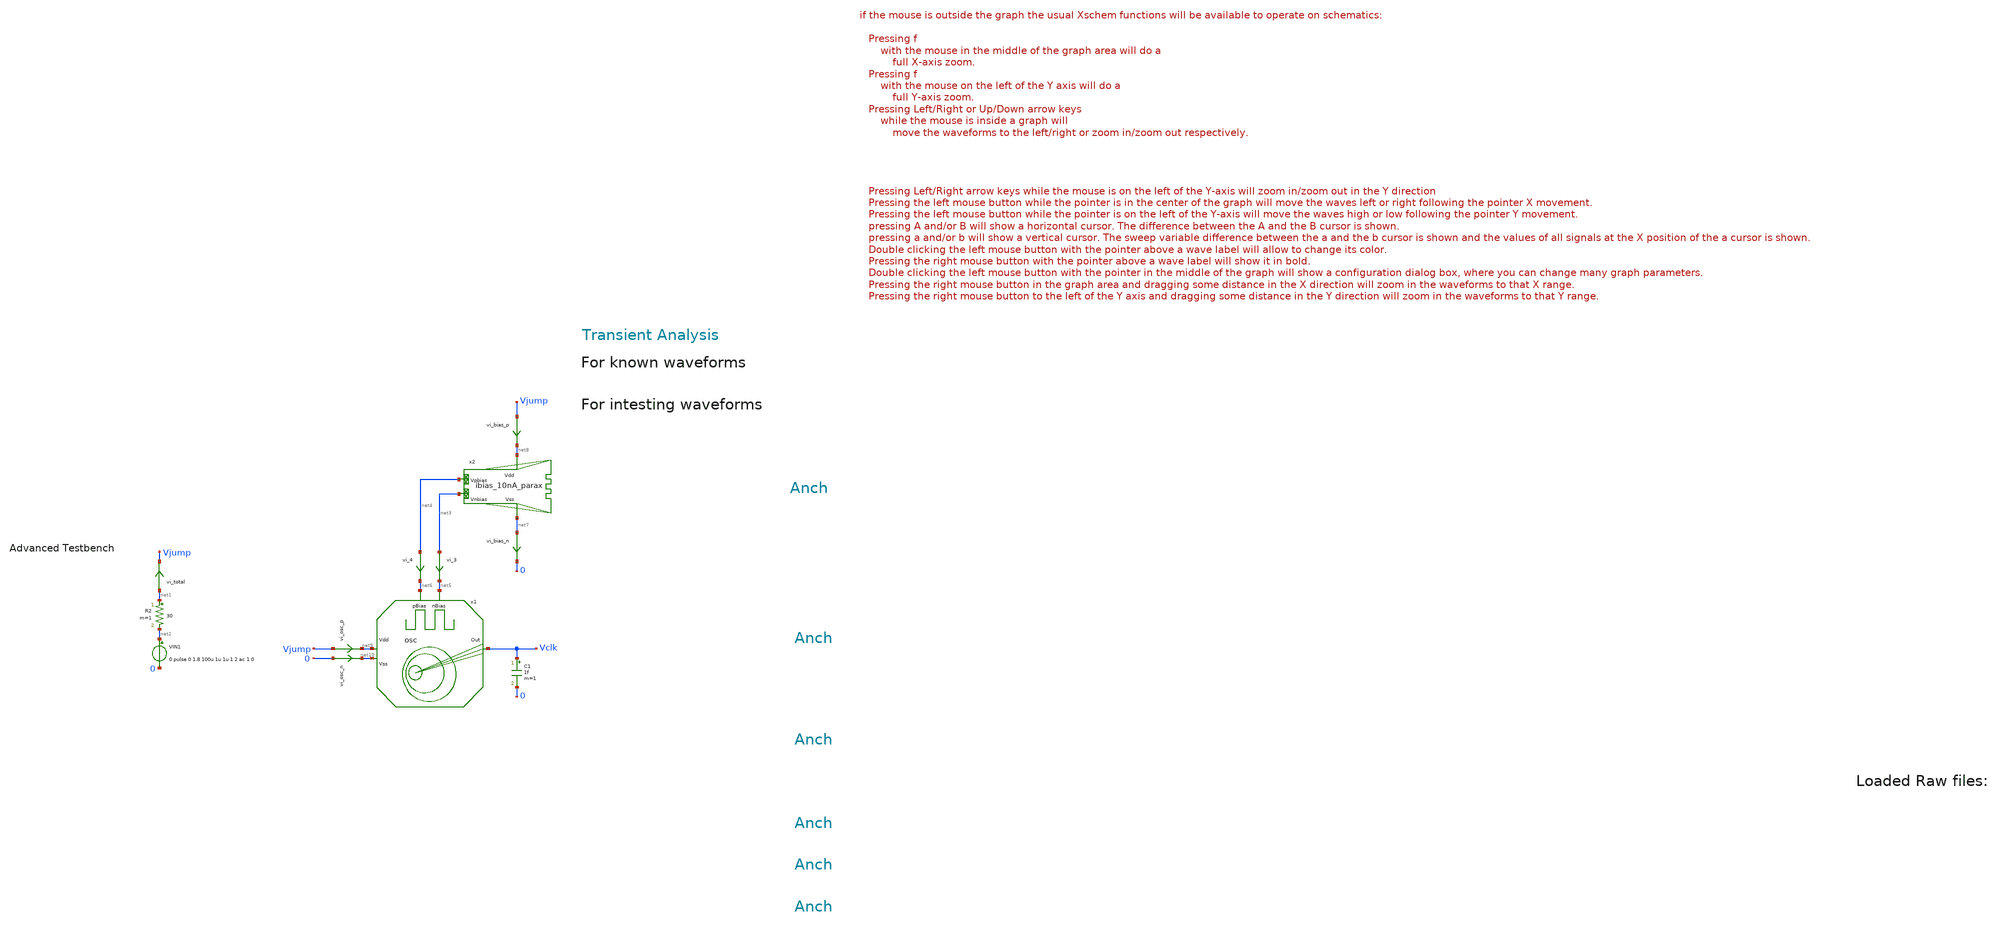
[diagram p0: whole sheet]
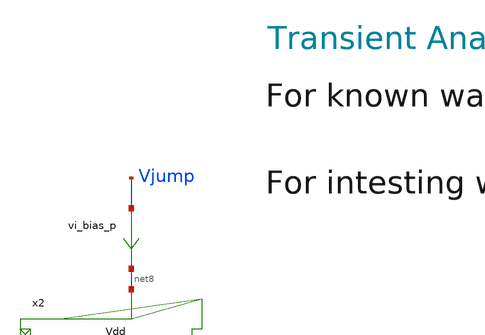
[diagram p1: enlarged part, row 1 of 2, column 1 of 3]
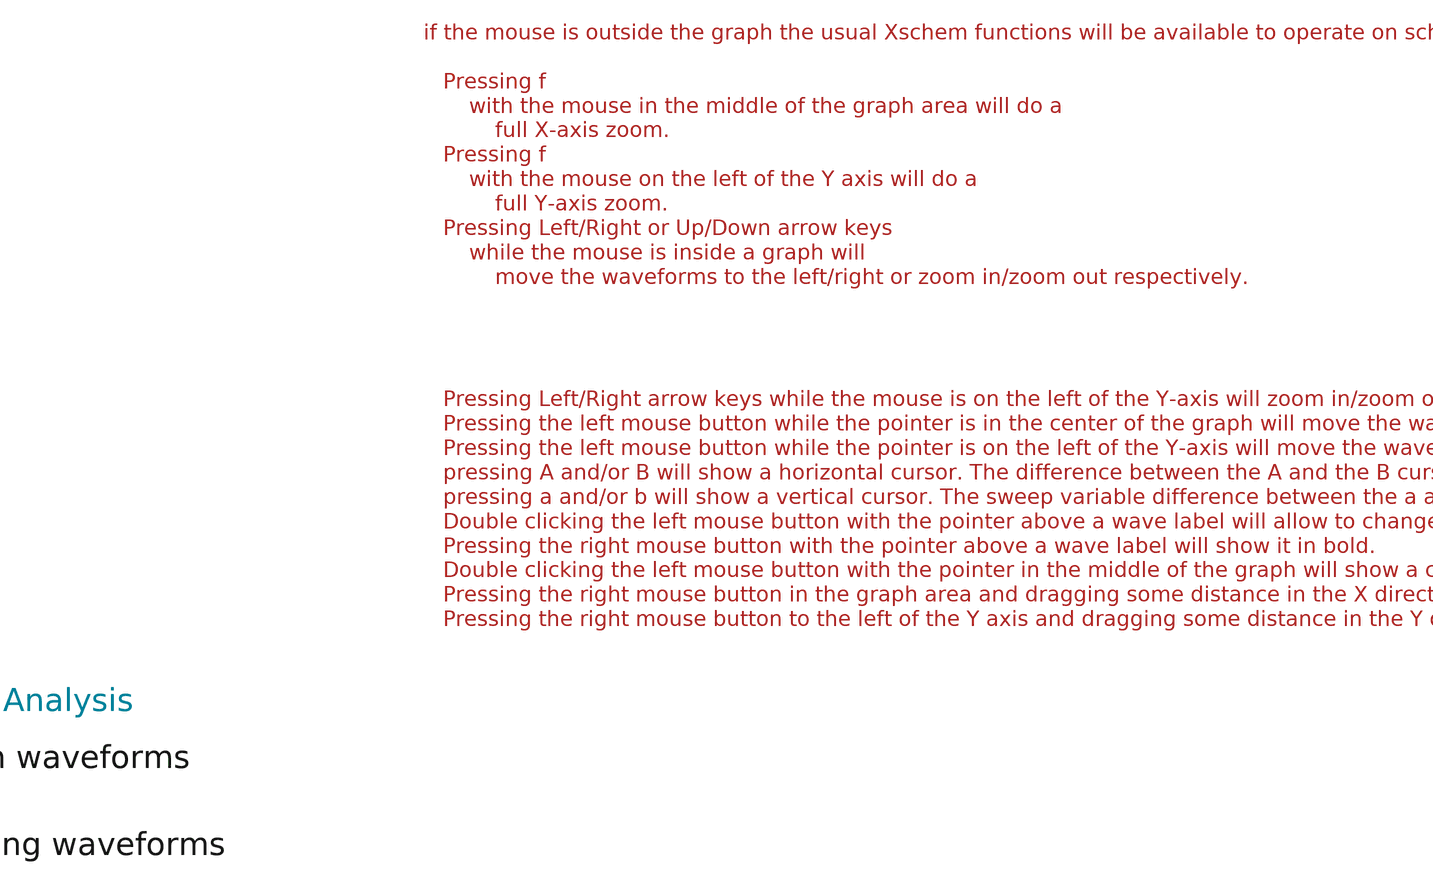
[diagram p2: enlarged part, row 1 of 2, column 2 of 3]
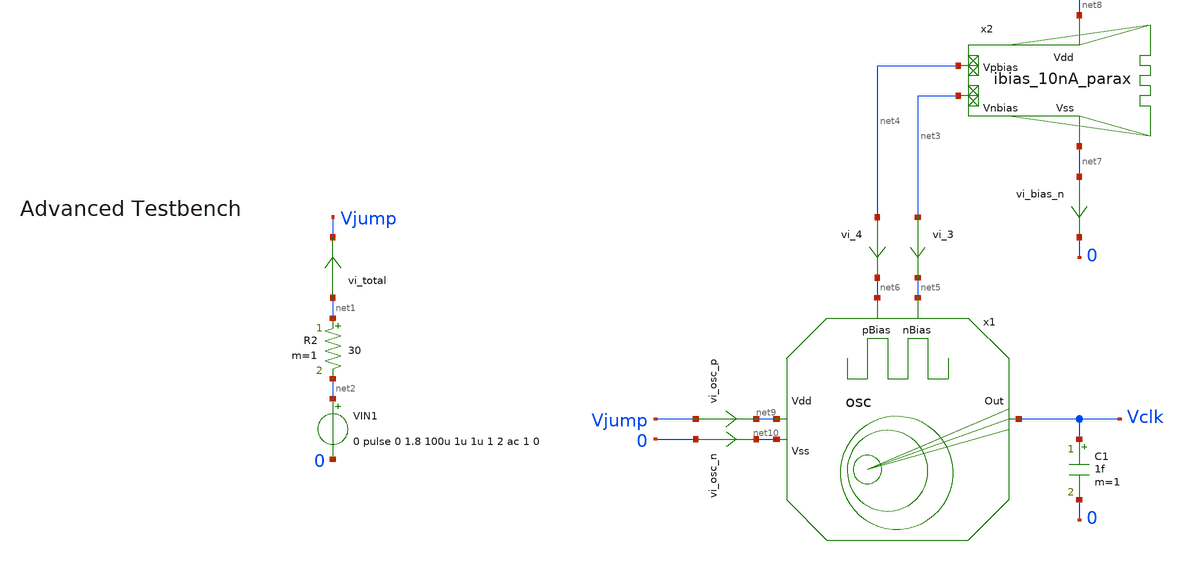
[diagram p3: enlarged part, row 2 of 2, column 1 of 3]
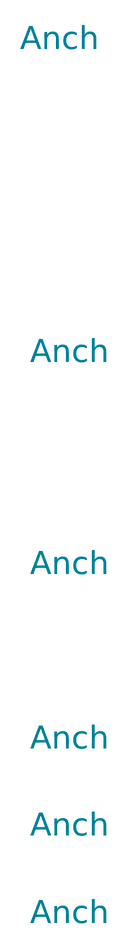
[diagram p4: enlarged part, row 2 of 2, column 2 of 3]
** sch_path: tt10-hdl/tt_um_test_commit/xschem/T3/oscillators/A_tt10_Ring_currentStarved/osc_general_tran_tb.sch
* Copyright (C) 1998-2024 Stefan Frederik Schippers
* This program is free software; you can redistribute it and/or modify
* it under the terms of the GNU General Public License as published by
* the Free Software Foundation; either version 2 of the License, or
* (at your option) any later version.
* This program is distributed in the hope that it will be useful,
* but WITHOUT ANY WARRANTY; without even the implied warranty of
* MERCHANTABILITY or FITNESS FOR A PARTICULAR PURPOSE.  See the
* GNU General Public License for more details.
* You should have received a copy of the GNU General Public License
* along with this program; if not, write to the Free Software
**.subckt osc_general_tran_tb
VIN1 net2 0 0 pulse 0 1.8 100u 1u 1u 1 2 ac 1 0
vi_total net1 Vjump 0
.save i(vi_total)
R2 net1 net2 30 m=1
C1 Vclk 0 1f m=1
x1 net9 net10 net6 Vclk net5 osc
vi_bias_n net7 0 0
.save i(vi_bias_n)
vi_bias_p Vjump net8 0
.save i(vi_bias_p)
vi_3 net3 net5 0
.save i(vi_3)
vi_4 net4 net6 0
.save i(vi_4)
vi_osc_p Vjump net9 0
.save i(vi_osc_p)
vi_osc_n 0 net10 0
.save i(vi_osc_n)
x2 net8 net7 net3 net4 ibias_10nA_parax
**** begin user architecture code



.temp 30
.param Vdd = 1.8
.param imax = 100e-9


.option savecurrents
.save all
.control
  save all alli
  save

  op
  write osc_51k5Hz_tb.raw
  remzerovec
  set appendwrite

  tran 0.1u 1.5m
  remzerovec
  write osc_51k5Hz_tb.raw





  *quit 0




.endc





** opencircuitdesign pdks install
.lib $::SKYWATER_MODELS/sky130.lib.spice tt


**** end user architecture code
**.ends

* expanding   symbol:  T3/oscillators/A_tt10_Ring_currentStarved/osc.sym # of pins=5
** sym_path: tt10-hdl/tt_um_test_commit/xschem/T3/oscillators/A_tt10_Ring_currentStarved/osc.sym
** sch_path: tt10-hdl/tt_um_test_commit/xschem/T3/oscillators/A_tt10_Ring_currentStarved/osc.sch
.subckt osc Vdd Vss pBias Out nBias
*.ipin Vdd
*.ipin Vss
*.opin Out
*.ipin nBias
*.ipin pBias
XM6 net1 nBias Vss Vss sky130_fd_pr__nfet_01v8 L=0.4 W=2.25 nf=1 ad='int((1 + 1)/2) * 2.25 / 1 * 0.29'
+ as='int((1 + 2)/2) * 2.25 / 1 * 0.29' pd='2*int((1 + 1)/2) * (2.25 / 1 + 0.29)' ps='2*int((1 + 2)/2) * (2.25 / 1 + 0.29)'
+ nrd='0.29 / 2.25 ' nrs='0.29 / 2.25 ' sa=0 sb=0 sd=0 mult=1 m=1
XM7 net4 pBias Vdd Vdd sky130_fd_pr__pfet_01v8 L=0.35 W=1 nf=1 ad='int((nf+1)/2) * W/nf * 0.29' as='int((nf+2)/2) * W/nf * 0.29'
+ pd='2*int((nf+1)/2) * (W/nf + 0.29)' ps='2*int((nf+2)/2) * (W/nf + 0.29)' nrd='0.29 / W' nrs='0.29 / W'
+ sa=0 sb=0 sd=0 mult=1 m=1
XM8 net2 nBias Vss Vss sky130_fd_pr__nfet_01v8 L=0.4 W=2.25 nf=1 ad='int((1 + 1)/2) * 2.25 / 1 * 0.29'
+ as='int((1 + 2)/2) * 2.25 / 1 * 0.29' pd='2*int((1 + 1)/2) * (2.25 / 1 + 0.29)' ps='2*int((1 + 2)/2) * (2.25 / 1 + 0.29)'
+ nrd='0.29 / 2.25 ' nrs='0.29 / 2.25 ' sa=0 sb=0 sd=0 mult=1 m=1
XM9 net5 pBias Vdd Vdd sky130_fd_pr__pfet_01v8 L=0.35 W=1 nf=1 ad='int((nf+1)/2) * W/nf * 0.29' as='int((nf+2)/2) * W/nf * 0.29'
+ pd='2*int((nf+1)/2) * (W/nf + 0.29)' ps='2*int((nf+2)/2) * (W/nf + 0.29)' nrd='0.29 / W' nrs='0.29 / W'
+ sa=0 sb=0 sd=0 mult=1 m=1
XM10 net3 nBias Vss Vss sky130_fd_pr__nfet_01v8 L=0.4 W=2.25 nf=1 ad='int((1 + 1)/2) * 2.25 / 1 * 0.29'
+ as='int((1 + 2)/2) * 2.25 / 1 * 0.29' pd='2*int((1 + 1)/2) * (2.25 / 1 + 0.29)' ps='2*int((1 + 2)/2) * (2.25 / 1 + 0.29)'
+ nrd='0.29 / 2.25 ' nrs='0.29 / 2.25 ' sa=0 sb=0 sd=0 mult=1 m=1
XM11 net6 pBias Vdd Vdd sky130_fd_pr__pfet_01v8 L=0.35 W=1 nf=1 ad='int((nf+1)/2) * W/nf * 0.29' as='int((nf+2)/2) * W/nf * 0.29'
+ pd='2*int((nf+1)/2) * (W/nf + 0.29)' ps='2*int((nf+2)/2) * (W/nf + 0.29)' nrd='0.29 / W' nrs='0.29 / W'
+ sa=0 sb=0 sd=0 mult=1 m=1
x2 net10 net2 net5 net11 Vdd Vss schmTrigg
x1 net7 net1 net4 net10 Vdd Vss schmTrigg
x4 net11 net3 net6 net7 Vdd Vss schmTrigg
XM1 net8 nBias Vss Vss sky130_fd_pr__nfet_01v8 L=0.4 W=2.25 nf=1 ad='int((1 + 1)/2) * 2.25 / 1 * 0.29'
+ as='int((1 + 2)/2) * 2.25 / 1 * 0.29' pd='2*int((1 + 1)/2) * (2.25 / 1 + 0.29)' ps='2*int((1 + 2)/2) * (2.25 / 1 + 0.29)'
+ nrd='0.29 / 2.25 ' nrs='0.29 / 2.25 ' sa=0 sb=0 sd=0 mult=1 m=1
XM3 net9 pBias Vdd Vdd sky130_fd_pr__pfet_01v8 L=0.35 W=1 nf=1 ad='int((nf+1)/2) * W/nf * 0.29' as='int((nf+2)/2) * W/nf * 0.29'
+ pd='2*int((nf+1)/2) * (W/nf + 0.29)' ps='2*int((nf+2)/2) * (W/nf + 0.29)' nrd='0.29 / W' nrs='0.29 / W'
+ sa=0 sb=0 sd=0 mult=1 m=1
x5 net7 net8 net9 Out Vdd Vss schmTrigg
XC1 net10 Vss sky130_fd_pr__cap_mim_m3_1 W=5 L=5 MF=1 m=1
XC2 net11 Vss sky130_fd_pr__cap_mim_m3_1 W=5 L=5 MF=1 m=1
XC3 net7 Vss sky130_fd_pr__cap_mim_m3_1 W=5 L=5 MF=1 m=1
.ends


* expanding   symbol:  T2/biasGen/A_tt10_10nA/ibias_10nA_parax.sym # of pins=4
** sym_path: tt10-hdl/tt_um_test_commit/xschem/T2/biasGen/A_tt10_10nA/ibias_10nA_parax.sym
.include T2/biasGen/A_tt10_10nA/ibias_10nA_parax.spice

* expanding   symbol:  T1/schmTrigg/schmTrigg.sym # of pins=6
** sym_path: tt10-hdl/tt_um_test_commit/xschem/T1/schmTrigg/schmTrigg.sym
** sch_path: tt10-hdl/tt_um_test_commit/xschem/T1/schmTrigg/schmTrigg.sch
.subckt schmTrigg Vin VSS VDD Vout pBulk nBulk
*.ipin Vin
*.ipin VDD
*.ipin VSS
*.opin Vout
*.ipin nBulk
*.ipin pBulk
XM1 VDD Vout Vn nBulk sky130_fd_pr__nfet_01v8 L=0.15 W=1 nf=1 ad='int((1 + 1)/2) * 1 / 1 * 0.29' as='int((1 + 2)/2) * 1 / 1 * 0.29'
+ pd='2*int((1 + 1)/2) * (1 / 1 + 0.29)' ps='2*int((1 + 2)/2) * (1 / 1 + 0.29)' nrd='0.29 / 1 ' nrs='0.29 / 1 '
+ sa=0 sb=0 sd=0 mult=1 m=1
XM2 Vn Vin VSS nBulk sky130_fd_pr__nfet_01v8 L=0.15 W=1 nf=1 ad='int((1 + 1)/2) * 1 / 1 * 0.29' as='int((1 + 2)/2) * 1 / 1 * 0.29'
+ pd='2*int((1 + 1)/2) * (1 / 1 + 0.29)' ps='2*int((1 + 2)/2) * (1 / 1 + 0.29)' nrd='0.29 / 1 ' nrs='0.29 / 1 '
+ sa=0 sb=0 sd=0 mult=1 m=1
XM3 Vout Vin Vn nBulk sky130_fd_pr__nfet_01v8 L=0.15 W=1 nf=1 ad='int((1 + 1)/2) * 1 / 1 * 0.29' as='int((1 + 2)/2) * 1 / 1 * 0.29'
+ pd='2*int((1 + 1)/2) * (1 / 1 + 0.29)' ps='2*int((1 + 2)/2) * (1 / 1 + 0.29)' nrd='0.29 / 1 ' nrs='0.29 / 1 '
+ sa=0 sb=0 sd=0 mult=1 m=1
XM4 VSS Vout Vp pBulk sky130_fd_pr__pfet_01v8 L=0.15 W=1 nf=1 ad='int((nf+1)/2) * W/nf * 0.29' as='int((nf+2)/2) * W/nf * 0.29'
+ pd='2*int((nf+1)/2) * (W/nf + 0.29)' ps='2*int((nf+2)/2) * (W/nf + 0.29)' nrd='0.29 / W' nrs='0.29 / W'
+ sa=0 sb=0 sd=0 mult=1 m=1
XM5 Vout Vin Vp pBulk sky130_fd_pr__pfet_01v8 L=0.15 W=1 nf=1 ad='int((nf+1)/2) * W/nf * 0.29' as='int((nf+2)/2) * W/nf * 0.29'
+ pd='2*int((nf+1)/2) * (W/nf + 0.29)' ps='2*int((nf+2)/2) * (W/nf + 0.29)' nrd='0.29 / W' nrs='0.29 / W'
+ sa=0 sb=0 sd=0 mult=1 m=1
XM6 Vp Vin VDD pBulk sky130_fd_pr__pfet_01v8 L=0.15 W=1 nf=1 ad='int((nf+1)/2) * W/nf * 0.29' as='int((nf+2)/2) * W/nf * 0.29'
+ pd='2*int((nf+1)/2) * (W/nf + 0.29)' ps='2*int((nf+2)/2) * (W/nf + 0.29)' nrd='0.29 / W' nrs='0.29 / W'
+ sa=0 sb=0 sd=0 mult=1 m=1
.ends

.end
